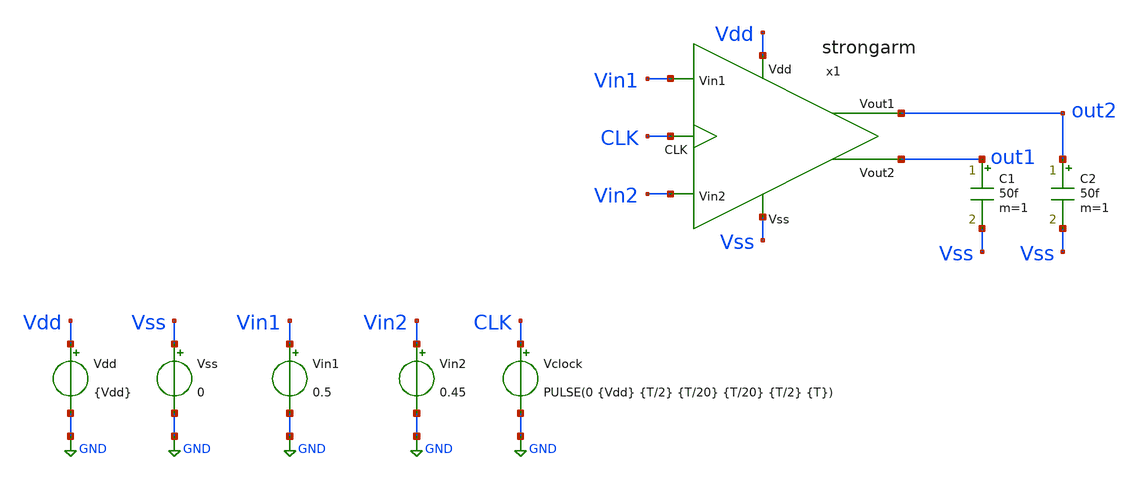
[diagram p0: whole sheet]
** sch_path: xschem/TB/TB_strongarm.sch
**.subckt TB_strongarm
Vdd Vdd GND {Vdd}
x1 out1 out2 Vdd Vss Vin2 Vin1 CLK strongarm
Vss Vss GND 0
C1 out1 Vss 50f m=1
C2 out2 Vss 50f m=1
Vin1 Vin1 GND 0.5
Vin2 Vin2 GND 0.45
Vclock CLK GND PULSE(0 {Vdd} {T/2} {T/20} {T/20} {T/2} {T})
**** begin user architecture code


.param Vdd = 1.2






.lib cornerMOSlv.lib mos_tt




** TRANSISTORES NMOS

.param W12 = 1.0u
.param L12 = 0.13u
.param M12 = 1

.param W34 = 1.0u
.param L34 = 0.13u
.param M34 = 1

.param W56 = 1.0u
.param L56 = 0.13u
.param M56 = 1

.param W7  = 1.0u
.param L7  = 0.13u
.param M7  = 1

.param W89 = 1.0u
.param L89 = 0.13u
.param M89 = 1

.param Wab = 1.0u
.param Lab = 0.13u
.param Mab = 1









.control
.param T = 1u
.param SimTime = 3*T + 100n
save all  @n.x1.xm1.nsg13_lv_nmos[gm]  @n.x1.xm2.nsg13_lv_nmos[gm]  @n.x1.xm1.nsg13_lv_nmos[ids]
+  @n.x1.xm2.nsg13_lv_nmos[ids]
tran 1n {SimTime}
plot v(out1) v(out2)
.endc


**** end user architecture code
**.ends

* expanding   symbol:  ../sch/strongarm.sym # of pins=7
** sym_path: xschem/sch/strongarm.sym
** sch_path: xschem/sch/strongarm.sch
.subckt strongarm Vout2 Vout1 Vdd Vss Vin2 Vin1 CLK
*.opin Vout2
*.opin Vout1
*.ipin Vin1
*.ipin Vin2
*.ipin CLK
*.ipin Vss
*.ipin Vdd
XM1 common Vin1 P Vss sg13_lv_nmos w={W12} l={L12} ng={F12} m={M12} mm_ok=1
XM2 common Vin2 Q Vss sg13_lv_nmos w={W12} l={L12} ng={F12} m={M12} mm_ok=1
XM3 P Vout2 Vout1 Vss sg13_lv_nmos w={W34} l={L34} ng={F34} m={M34} mm_ok=1
XM4 Q Vout1 Vout2 Vss sg13_lv_nmos w={W34} l={L34} ng={F34} m={M34} mm_ok=1
XM6 Vout2 Vout1 Vdd Vdd sg13_lv_pmos w={W56} l={L56} ng={F56} m={M56} mm_ok=1
XM5 Vout1 Vout2 Vdd Vdd sg13_lv_pmos w={W56} l={L56} ng={F56} m={M56} mm_ok=1
XM7 Vss CLK common Vss sg13_lv_nmos w={W7} l={L7} ng={F7} m={M7} mm_ok=1
XM8 P CLK Vdd Vdd sg13_lv_pmos w={W89} l={L89} ng={F89} m={M89} mm_ok=1
XM9 Q CLK Vdd Vdd sg13_lv_pmos w={W89} l={L89} ng={F89} m={M89} mm_ok=1
XM11 Vdd CLK Vout2 Vdd sg13_lv_pmos w={Wab} l={Lab} ng={Fab} m={Mab} mm_ok=1
XM10 Vdd CLK Vout1 Vdd sg13_lv_pmos w={Wab} l={Lab} ng={Fab} m={Mab} mm_ok=1
.ends

.GLOBAL GND
.end
